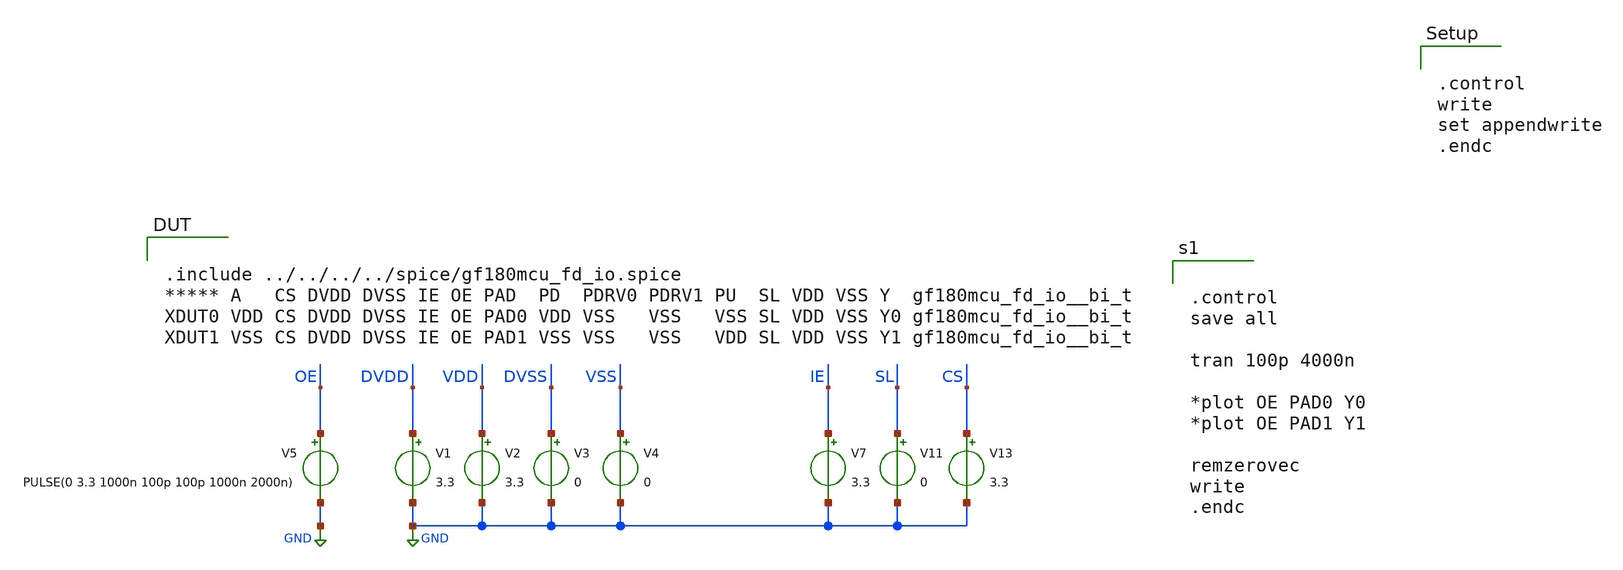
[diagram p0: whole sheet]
** sch_path: padframe/switching_bi_t_tristate/test/switching_bi_t_tristate.sch

.control
write
set appendwrite
.endc

.include $env(PDK_ROOT)/$env(PDK)/libs.tech/ngspice/design.ngspice
.lib $env(PDK_ROOT)/$env(PDK)/libs.tech/ngspice/sm141064.ngspice typical
.lib $env(PDK_ROOT)/$env(PDK)/libs.tech/ngspice/sm141064.ngspice diode_typical
.lib $env(PDK_ROOT)/$env(PDK)/libs.tech/ngspice/sm141064.ngspice res_typical
.lib $env(PDK_ROOT)/$env(PDK)/libs.tech/ngspice/sm141064.ngspice mimcap_typical
.lib $env(PDK_ROOT)/$env(PDK)/libs.tech/ngspice/sm141064.ngspice moscap_typical
.lib $env(PDK_ROOT)/$env(PDK)/libs.tech/ngspice/sm141064.ngspice bjt_typical
*.lib $env(PDK_ROOT)/$env(PDK)/libs.tech/ngspice/sm141064.ngspice cap_mim

**.subckt switching_bi_t_tristate
V1 DVDD GND 3.3
V2 VDD GND 3.3
V3 DVSS GND 0
V4 VSS GND 0
V5 OE GND PULSE(0 3.3 1000n 100p 100p 1000n 2000n)
V7 IE GND 3.3
V11 SL GND 0
V13 CS GND 3.3
**** begin user architecture code


.control
save all

tran 100p 4000n

*plot OE PAD0 Y0
*plot OE PAD1 Y1

remzerovec
write
.endc



.include ../../../../spice/gf180mcu_fd_io.spice
***** A   CS DVDD DVSS IE OE PAD  PD  PDRV0 PDRV1 PU  SL VDD VSS Y  gf180mcu_fd_io__bi_t
XDUT0 VDD CS DVDD DVSS IE OE PAD0 VDD VSS   VSS   VSS SL VDD VSS Y0 gf180mcu_fd_io__bi_t
XDUT1 VSS CS DVDD DVSS IE OE PAD1 VSS VSS   VSS   VDD SL VDD VSS Y1 gf180mcu_fd_io__bi_t

**** end user architecture code
**.ends
.GLOBAL GND
.end
